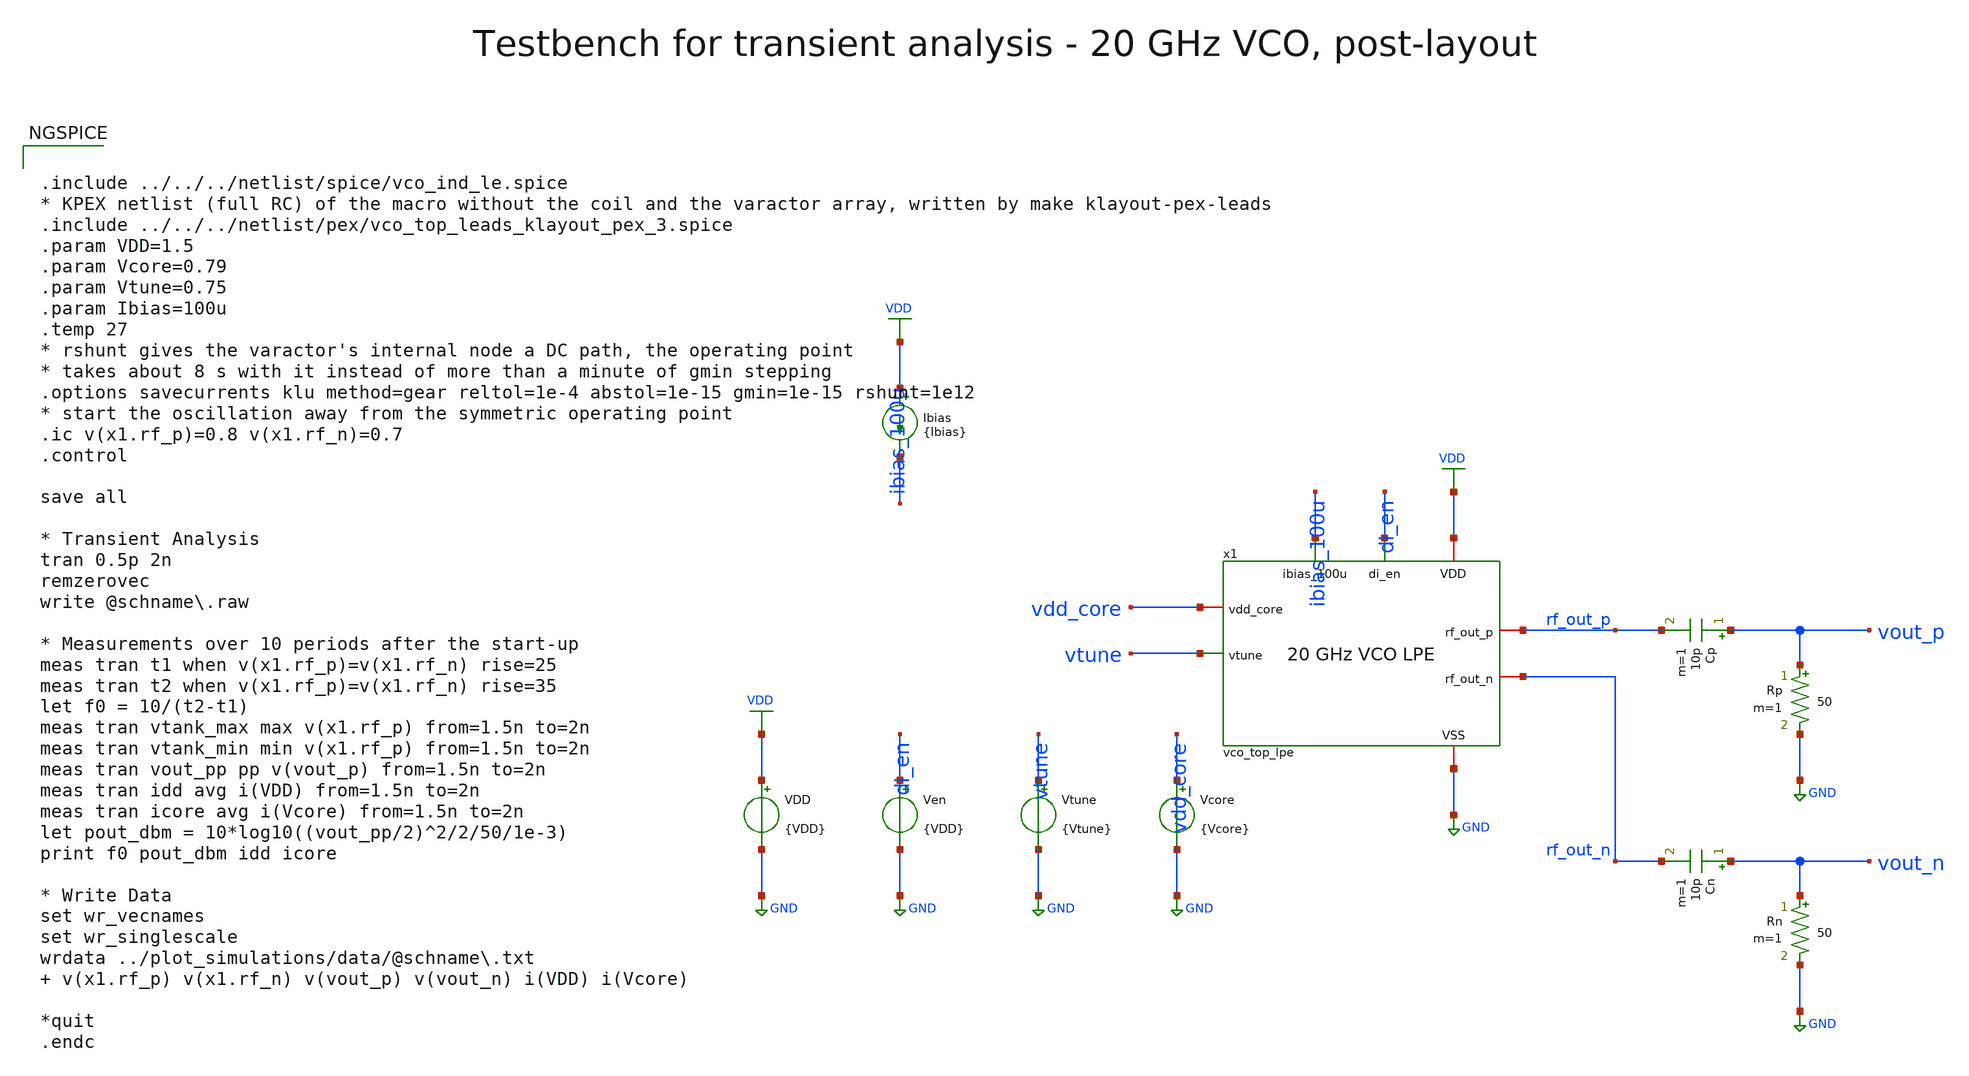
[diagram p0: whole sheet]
** sch_path: macros/vco/testbenches/xschem/vco_top_tb_tran_lpe.sch
**.subckt vco_top_tb_tran_lpe
x1 ibias_100u di_en VDD GND vdd_core vtune rf_out_p rf_out_n vco_top_lpe
Vcore vdd_core GND {Vcore}
Cp vout_p rf_out_p 10p m=1
Rp vout_p GND 50 m=1
Cn vout_n rf_out_n 10p m=1
Rn vout_n GND 50 m=1
VDD VDD GND {VDD}
Ven di_en GND {VDD}
Vtune vtune GND {Vtune}
Ibias VDD ibias_100u {Ibias}
**** begin user architecture code


.include ../../../netlist/spice/vco_ind_le.spice
* KPEX netlist (full RC) of the macro without the coil and the varactor array, written by make
*+ klayout-pex-leads
.include ../../../netlist/pex/vco_top_leads_klayout_pex_3.spice
.param VDD=1.5
.param Vcore=0.79
.param Vtune=0.75
.param Ibias=100u
.temp 27
* rshunt gives the varactor's internal node a DC path, the operating point
* takes about 8 s with it instead of more than a minute of gmin stepping
.options savecurrents klu method=gear reltol=1e-4 abstol=1e-15 gmin=1e-15 rshunt=1e12
* start the oscillation away from the symmetric operating point
.ic v(x1.rf_p)=0.8 v(x1.rf_n)=0.7
.control

save all

* Transient Analysis
tran 0.5p 2n
remzerovec
write @schname\.raw

* Measurements over 10 periods after the start-up
meas tran t1 when v(x1.rf_p)=v(x1.rf_n) rise=25
meas tran t2 when v(x1.rf_p)=v(x1.rf_n) rise=35
let f0 = 10/(t2-t1)
meas tran vtank_max max v(x1.rf_p) from=1.5n to=2n
meas tran vtank_min min v(x1.rf_p) from=1.5n to=2n
meas tran vout_pp pp v(vout_p) from=1.5n to=2n
meas tran idd avg i(VDD) from=1.5n to=2n
meas tran icore avg i(Vcore) from=1.5n to=2n
let pout_dbm = 10*log10((vout_pp/2)^2/2/50/1e-3)
print f0 pout_dbm idd icore

* Write Data
set wr_vecnames
set wr_singlescale
wrdata ../plot_simulations/data/@schname\.txt  v(x1.rf_p) v(x1.rf_n) v(vout_p) v(vout_n) i(VDD) i(Vcore)

*quit
.endc



.lib cornerMOSlv.lib mos_tt
.lib cornerMOShv.lib mos_tt
.lib cornerRES.lib res_typ
.lib cornerCAP.lib cap_typ

**** end user architecture code
**.ends

* expanding   symbol:  vco_top_lpe.sym # of pins=8
** sym_path: macros/vco/testbenches/xschem/vco_top_lpe.sym
** sch_path: macros/vco/testbenches/xschem/vco_top_lpe.sch
.subckt vco_top_lpe ibias_100u di_en VDD VSS vdd_core vtune rf_out_p rf_out_n
*.iopin VDD
*.iopin VSS
*.iopin vdd_core
*.ipin ibias_100u
*.ipin di_en
*.ipin vtune
*.iopin rf_out_p
*.iopin rf_out_n
xleads ibias_100u di_en vtune VDD vdd_core VSS rf_out_p rf_out_n rf_p rf_n vco_ind_LC vco_var_rf_p vco_var_rf_n vco_var_VSS vco_top_leads
xind rf_p rf_n vco_ind_LC vco_ind_le
xvar vco_var_rf_p vco_var_rf_n vtune vco_var_VSS vco_var
.ends


* expanding   symbol:  vco_var.sym # of pins=4
** sym_path: macros/vco/schematic/xschem/vco_var.sym
** sch_path: macros/vco/schematic/xschem/vco_var.sch
.subckt vco_var rf_p rf_n vtune VSS
*.ipin vtune
*.iopin rf_p
*.iopin rf_n
*.iopin VSS
XCvar1 rf_p vtune rf_n VSS sg13_hv_svaricap w=3.74u l=0.3u Nx=7 mm_ok=1
XCvar2 rf_p vtune rf_n VSS sg13_hv_svaricap w=3.74u l=0.3u Nx=7 mm_ok=1
XCvar3 rf_p vtune rf_n VSS sg13_hv_svaricap w=3.74u l=0.3u Nx=7 mm_ok=1
.ends

.GLOBAL VDD
.GLOBAL GND
.end
